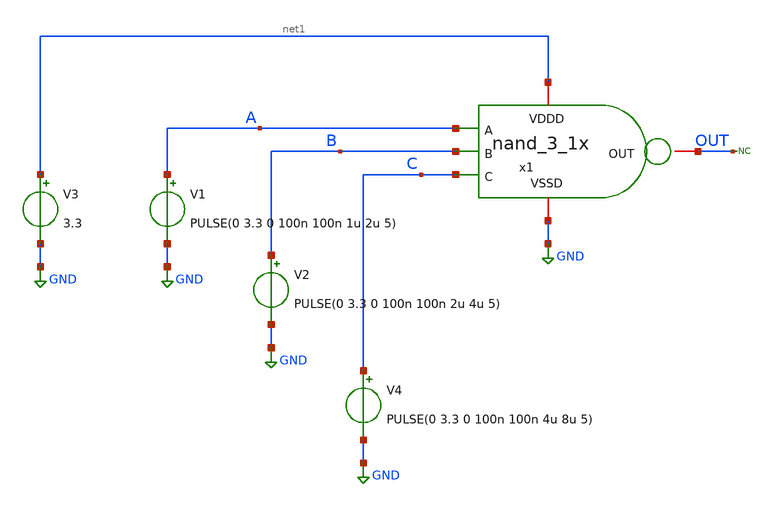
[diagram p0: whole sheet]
** sch_path: SAR_ADC/blocks/SAR_logic/nand_3_1x_tb.sch
**.subckt nand_3_1x_tb
* noconn OUT
V1 A GND PULSE(0 3.3 0 100n 100n 1u 2u 5)
V2 B GND PULSE(0 3.3 0 100n 100n 2u 4u 5)
V3 net1 GND 3.3
x1 C net1 OUT A B GND nand_3_1x
V4 C GND PULSE(0 3.3 0 100n 100n 4u 8u 5)
**** begin user architecture code



*Parameters
.options TEMPS= 27.0

*Models
.include /home/electrica/Documents/gf180_projects/pdk/gf180mcuC/libs.tech/ngspice/design.ngspice
.lib /home/electrica/Documents/gf180_projects/pdk/gf180mcuC/libs.tech/ngspice/sm141064.ngspice typical
.lib /home/electrica/Documents/gf180_projects/pdk/gf180mcuC/libs.tech/ngspice/smbb000149.ngspice typical


*Data to save
.save all

*Simulation
.control
tran 1n 20u
setplot dc1
plot V(A) V(B) V(OUT)
set filetype=ascii
write nand_2_1x_tb_1.raw

reset
unset filetype
op
save all
write nand_2_1x_tb.raw

.endc
.end



**** end user architecture code
**.ends

* expanding   symbol:
*+  /home/electrica/Documents/gf180_projects/gf180_work/PICO_contest/SAR_logic/nand_3_1x.sym # of pins=6
** sym_path: SAR_ADC/SAR_logic/xschem/nand_3_1x.sym
** sch_path: SAR_ADC/SAR_logic/xschem/nand_3_1x.sch
.subckt nand_3_1x C VDDD OUT A B VSSD
*.ipin A
*.ipin B
*.ipin C
*.iopin VDDD
*.iopin VSSD
*.iopin OUT
XM1 OUT A net1 VSSD nfet_03v3 L=0.28u W=0.22u nf=1 ad='int((nf+1)/2) * W/nf * 0.18u' as='int((nf+2)/2) * W/nf * 0.18u'
+ pd='2*int((nf+1)/2) * (W/nf + 0.18u)' ps='2*int((nf+2)/2) * (W/nf + 0.18u)' nrd='0.18u / W' nrs='0.18u / W'
+ sa=0 sb=0 sd=0 m=1
XM2 net1 B net2 VSSD nfet_03v3 L=0.28u W=0.22u nf=1 ad='int((nf+1)/2) * W/nf * 0.18u' as='int((nf+2)/2) * W/nf * 0.18u'
+ pd='2*int((nf+1)/2) * (W/nf + 0.18u)' ps='2*int((nf+2)/2) * (W/nf + 0.18u)' nrd='0.18u / W' nrs='0.18u / W'
+ sa=0 sb=0 sd=0 m=1
XM3 net2 C VSSD VSSD nfet_03v3 L=0.28u W=0.22u nf=1 ad='int((nf+1)/2) * W/nf * 0.18u' as='int((nf+2)/2) * W/nf * 0.18u'
+ pd='2*int((nf+1)/2) * (W/nf + 0.18u)' ps='2*int((nf+2)/2) * (W/nf + 0.18u)' nrd='0.18u / W' nrs='0.18u / W'
+ sa=0 sb=0 sd=0 m=1
XM4 OUT A VDDD VDDD pfet_03v3 L=0.28u W=0.22u nf=1 ad='int((nf+1)/2) * W/nf * 0.18u' as='int((nf+2)/2) * W/nf * 0.18u'
+ pd='2*int((nf+1)/2) * (W/nf + 0.18u)' ps='2*int((nf+2)/2) * (W/nf + 0.18u)' nrd='0.18u / W' nrs='0.18u / W'
+ sa=0 sb=0 sd=0 m=1
XM5 OUT B VDDD VDDD pfet_03v3 L=0.28u W=0.22u nf=1 ad='int((nf+1)/2) * W/nf * 0.18u' as='int((nf+2)/2) * W/nf * 0.18u'
+ pd='2*int((nf+1)/2) * (W/nf + 0.18u)' ps='2*int((nf+2)/2) * (W/nf + 0.18u)' nrd='0.18u / W' nrs='0.18u / W'
+ sa=0 sb=0 sd=0 m=1
XM6 OUT C VDDD VDDD pfet_03v3 L=0.28u W=0.22u nf=1 ad='int((nf+1)/2) * W/nf * 0.18u' as='int((nf+2)/2) * W/nf * 0.18u'
+ pd='2*int((nf+1)/2) * (W/nf + 0.18u)' ps='2*int((nf+2)/2) * (W/nf + 0.18u)' nrd='0.18u / W' nrs='0.18u / W'
+ sa=0 sb=0 sd=0 m=1
.ends

.GLOBAL GND
.end
